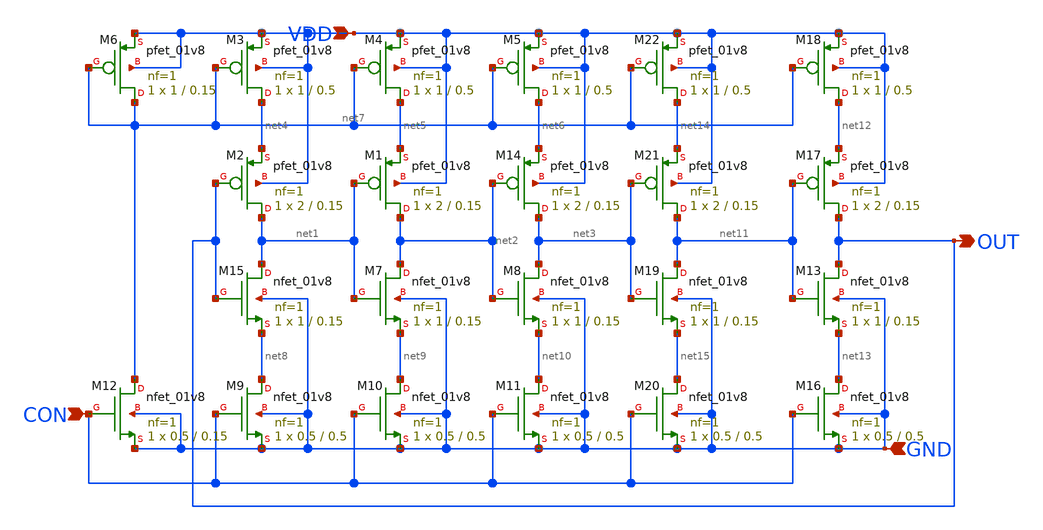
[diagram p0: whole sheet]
** sch_path: sch/VCO.sch
**.subckt VCO CON VDD GND OUT
*.ipin CON
*.ipin VDD
*.ipin GND
*.opin OUT
XM15 net1 OUT net8 GND sky130_fd_pr__nfet_01v8 L=0.15 W=1 nf=1 ad='int((1 + 1)/2) * 1 / 1 * 0.29' as='int((1 + 2)/2) * 1 / 1 * 0.29'
+ pd='2*int((1 + 1)/2) * (1 / 1 + 0.29)' ps='2*int((1 + 2)/2) * (1 / 1 + 0.29)' nrd='0.29 / 1 ' nrs='0.29 / 1 '
+ sa=0 sb=0 sd=0 mult=1 m=1
XM7 net2 net1 net9 GND sky130_fd_pr__nfet_01v8 L=0.15 W=1 nf=1 ad='int((1 + 1)/2) * 1 / 1 * 0.29' as='int((1 + 2)/2) * 1 / 1 * 0.29'
+ pd='2*int((1 + 1)/2) * (1 / 1 + 0.29)' ps='2*int((1 + 2)/2) * (1 / 1 + 0.29)' nrd='0.29 / 1 ' nrs='0.29 / 1 '
+ sa=0 sb=0 sd=0 mult=1 m=1
XM8 net3 net2 net10 GND sky130_fd_pr__nfet_01v8 L=0.15 W=1 nf=1 ad='int((1 + 1)/2) * 1 / 1 * 0.29' as='int((1 + 2)/2) * 1 / 1 * 0.29'
+ pd='2*int((1 + 1)/2) * (1 / 1 + 0.29)' ps='2*int((1 + 2)/2) * (1 / 1 + 0.29)' nrd='0.29 / 1 ' nrs='0.29 / 1 '
+ sa=0 sb=0 sd=0 mult=1 m=1
XM9 net8 CON GND GND sky130_fd_pr__nfet_01v8 L=0.5 W=0.5 nf=1 ad='int((1 + 1)/2) * 0.5 / 1 * 0.29' as='int((1 + 2)/2) * 0.5 / 1 * 0.29'
+ pd='2*int((1 + 1)/2) * (0.5 / 1 + 0.29)' ps='2*int((1 + 2)/2) * (0.5 / 1 + 0.29)' nrd='0.29 / 0.5 ' nrs='0.29 / 0.5 '
+ sa=0 sb=0 sd=0 mult=1 m=1
XM10 net9 CON GND GND sky130_fd_pr__nfet_01v8 L=0.5 W=0.5 nf=1 ad='int((1 + 1)/2) * 0.5 / 1 * 0.29' as='int((1 + 2)/2) * 0.5 / 1 * 0.29'
+ pd='2*int((1 + 1)/2) * (0.5 / 1 + 0.29)' ps='2*int((1 + 2)/2) * (0.5 / 1 + 0.29)' nrd='0.29 / 0.5 ' nrs='0.29 / 0.5 '
+ sa=0 sb=0 sd=0 mult=1 m=1
XM11 net10 CON GND GND sky130_fd_pr__nfet_01v8 L=0.5 W=0.5 nf=1 ad='int((1 + 1)/2) * 0.5 / 1 * 0.29'
+ as='int((1 + 2)/2) * 0.5 / 1 * 0.29' pd='2*int((1 + 1)/2) * (0.5 / 1 + 0.29)' ps='2*int((1 + 2)/2) * (0.5 / 1 + 0.29)'
+ nrd='0.29 / 0.5 ' nrs='0.29 / 0.5 ' sa=0 sb=0 sd=0 mult=1 m=1
XM12 net7 CON GND GND sky130_fd_pr__nfet_01v8 L=0.15 W=0.5 nf=1 ad='int((1 + 1)/2) * 0.5 / 1 * 0.29'
+ as='int((1 + 2)/2) * 0.5 / 1 * 0.29' pd='2*int((1 + 1)/2) * (0.5 / 1 + 0.29)' ps='2*int((1 + 2)/2) * (0.5 / 1 + 0.29)'
+ nrd='0.29 / 0.5 ' nrs='0.29 / 0.5 ' sa=0 sb=0 sd=0 mult=1 m=1
XM14 net3 net2 net6 VDD sky130_fd_pr__pfet_01v8 L=0.15 W=2 nf=1 ad='int((1 + 1)/2) * 2 / 1 * 0.29' as='int((1 + 2)/2) * 2 / 1 * 0.29'
+ pd='2*int((1 + 1)/2) * (2 / 1 + 0.29)' ps='2*int((1 + 2)/2) * (2 / 1 + 0.29)' nrd='0.29 / 2 ' nrs='0.29 / 2 '
+ sa=0 sb=0 sd=0 mult=1 m=1
XM1 net2 net1 net5 VDD sky130_fd_pr__pfet_01v8 L=0.15 W=2 nf=1 ad='int((1 + 1)/2) * 2 / 1 * 0.29' as='int((1 + 2)/2) * 2 / 1 * 0.29'
+ pd='2*int((1 + 1)/2) * (2 / 1 + 0.29)' ps='2*int((1 + 2)/2) * (2 / 1 + 0.29)' nrd='0.29 / 2 ' nrs='0.29 / 2 '
+ sa=0 sb=0 sd=0 mult=1 m=1
XM2 net1 OUT net4 VDD sky130_fd_pr__pfet_01v8 L=0.15 W=2 nf=1 ad='int((1 + 1)/2) * 2 / 1 * 0.29' as='int((1 + 2)/2) * 2 / 1 * 0.29'
+ pd='2*int((1 + 1)/2) * (2 / 1 + 0.29)' ps='2*int((1 + 2)/2) * (2 / 1 + 0.29)' nrd='0.29 / 2 ' nrs='0.29 / 2 '
+ sa=0 sb=0 sd=0 mult=1 m=1
XM3 net4 net7 VDD VDD sky130_fd_pr__pfet_01v8 L=0.5 W=1 nf=1 ad='int((1 + 1)/2) * 1 / 1 * 0.29' as='int((1 + 2)/2) * 1 / 1 * 0.29'
+ pd='2*int((1 + 1)/2) * (1 / 1 + 0.29)' ps='2*int((1 + 2)/2) * (1 / 1 + 0.29)' nrd='0.29 / 1 ' nrs='0.29 / 1 '
+ sa=0 sb=0 sd=0 mult=1 m=1
XM4 net5 net7 VDD VDD sky130_fd_pr__pfet_01v8 L=0.5 W=1 nf=1 ad='int((1 + 1)/2) * 1 / 1 * 0.29' as='int((1 + 2)/2) * 1 / 1 * 0.29'
+ pd='2*int((1 + 1)/2) * (1 / 1 + 0.29)' ps='2*int((1 + 2)/2) * (1 / 1 + 0.29)' nrd='0.29 / 1 ' nrs='0.29 / 1 '
+ sa=0 sb=0 sd=0 mult=1 m=1
XM5 net6 net7 VDD VDD sky130_fd_pr__pfet_01v8 L=0.5 W=1 nf=1 ad='int((1 + 1)/2) * 1 / 1 * 0.29' as='int((1 + 2)/2) * 1 / 1 * 0.29'
+ pd='2*int((1 + 1)/2) * (1 / 1 + 0.29)' ps='2*int((1 + 2)/2) * (1 / 1 + 0.29)' nrd='0.29 / 1 ' nrs='0.29 / 1 '
+ sa=0 sb=0 sd=0 mult=1 m=1
XM6 net7 net7 VDD VDD sky130_fd_pr__pfet_01v8 L=0.15 W=1 nf=1 ad='int((1 + 1)/2) * 1 / 1 * 0.29' as='int((1 + 2)/2) * 1 / 1 * 0.29'
+ pd='2*int((1 + 1)/2) * (1 / 1 + 0.29)' ps='2*int((1 + 2)/2) * (1 / 1 + 0.29)' nrd='0.29 / 1 ' nrs='0.29 / 1 '
+ sa=0 sb=0 sd=0 mult=1 m=1
XM13 OUT net11 net13 GND sky130_fd_pr__nfet_01v8 L=0.15 W=1 nf=1 ad='int((1 + 1)/2) * 1 / 1 * 0.29' as='int((1 + 2)/2) * 1 / 1 * 0.29'
+ pd='2*int((1 + 1)/2) * (1 / 1 + 0.29)' ps='2*int((1 + 2)/2) * (1 / 1 + 0.29)' nrd='0.29 / 1 ' nrs='0.29 / 1 '
+ sa=0 sb=0 sd=0 mult=1 m=1
XM16 net13 CON GND GND sky130_fd_pr__nfet_01v8 L=0.5 W=0.5 nf=1 ad='int((1 + 1)/2) * 0.5 / 1 * 0.29'
+ as='int((1 + 2)/2) * 0.5 / 1 * 0.29' pd='2*int((1 + 1)/2) * (0.5 / 1 + 0.29)' ps='2*int((1 + 2)/2) * (0.5 / 1 + 0.29)'
+ nrd='0.29 / 0.5 ' nrs='0.29 / 0.5 ' sa=0 sb=0 sd=0 mult=1 m=1
XM17 OUT net11 net12 VDD sky130_fd_pr__pfet_01v8 L=0.15 W=2 nf=1 ad='int((1 + 1)/2) * 2 / 1 * 0.29' as='int((1 + 2)/2) * 2 / 1 * 0.29'
+ pd='2*int((1 + 1)/2) * (2 / 1 + 0.29)' ps='2*int((1 + 2)/2) * (2 / 1 + 0.29)' nrd='0.29 / 2 ' nrs='0.29 / 2 '
+ sa=0 sb=0 sd=0 mult=1 m=1
XM18 net12 net7 VDD VDD sky130_fd_pr__pfet_01v8 L=0.5 W=1 nf=1 ad='int((1 + 1)/2) * 1 / 1 * 0.29' as='int((1 + 2)/2) * 1 / 1 * 0.29'
+ pd='2*int((1 + 1)/2) * (1 / 1 + 0.29)' ps='2*int((1 + 2)/2) * (1 / 1 + 0.29)' nrd='0.29 / 1 ' nrs='0.29 / 1 '
+ sa=0 sb=0 sd=0 mult=1 m=1
XM19 net11 net3 net15 GND sky130_fd_pr__nfet_01v8 L=0.15 W=1 nf=1 ad='int((1 + 1)/2) * 1 / 1 * 0.29'
+ as='int((1 + 2)/2) * 1 / 1 * 0.29' pd='2*int((1 + 1)/2) * (1 / 1 + 0.29)' ps='2*int((1 + 2)/2) * (1 / 1 + 0.29)'
+ nrd='0.29 / 1 ' nrs='0.29 / 1 ' sa=0 sb=0 sd=0 mult=1 m=1
XM20 net15 CON GND GND sky130_fd_pr__nfet_01v8 L=0.5 W=0.5 nf=1 ad='int((1 + 1)/2) * 0.5 / 1 * 0.29'
+ as='int((1 + 2)/2) * 0.5 / 1 * 0.29' pd='2*int((1 + 1)/2) * (0.5 / 1 + 0.29)' ps='2*int((1 + 2)/2) * (0.5 / 1 + 0.29)'
+ nrd='0.29 / 0.5 ' nrs='0.29 / 0.5 ' sa=0 sb=0 sd=0 mult=1 m=1
XM21 net11 net3 net14 VDD sky130_fd_pr__pfet_01v8 L=0.15 W=2 nf=1 ad='int((1 + 1)/2) * 2 / 1 * 0.29'
+ as='int((1 + 2)/2) * 2 / 1 * 0.29' pd='2*int((1 + 1)/2) * (2 / 1 + 0.29)' ps='2*int((1 + 2)/2) * (2 / 1 + 0.29)'
+ nrd='0.29 / 2 ' nrs='0.29 / 2 ' sa=0 sb=0 sd=0 mult=1 m=1
XM22 net14 net7 VDD VDD sky130_fd_pr__pfet_01v8 L=0.5 W=1 nf=1 ad='int((1 + 1)/2) * 1 / 1 * 0.29' as='int((1 + 2)/2) * 1 / 1 * 0.29'
+ pd='2*int((1 + 1)/2) * (1 / 1 + 0.29)' ps='2*int((1 + 2)/2) * (1 / 1 + 0.29)' nrd='0.29 / 1 ' nrs='0.29 / 1 '
+ sa=0 sb=0 sd=0 mult=1 m=1
**.ends
.end
